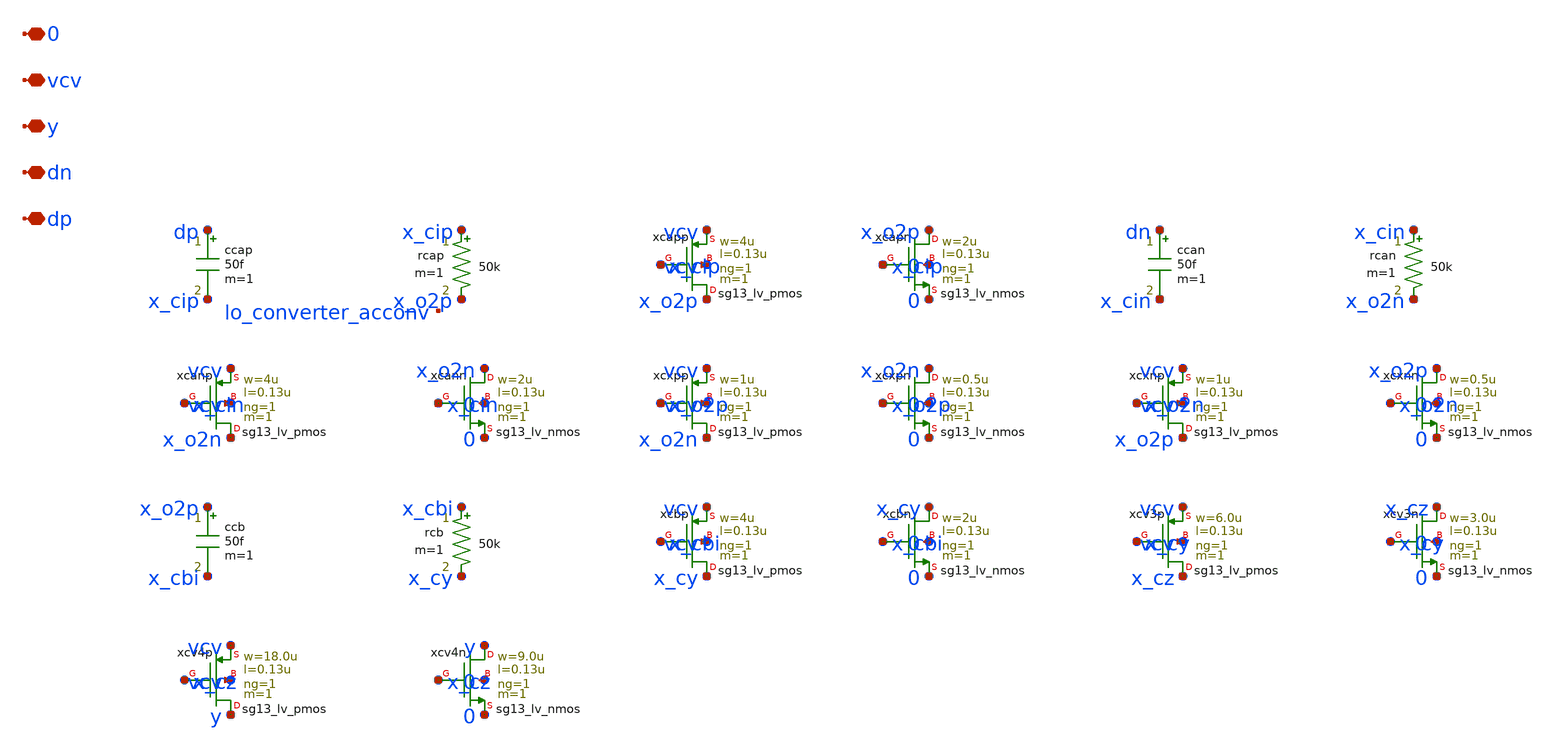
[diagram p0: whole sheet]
** sch_path: analog/lo/sch/lo_converter.sch
**.subckt lo_converter dp dn y vcv 0
*.iopin dp
*.iopin dn
*.iopin y
*.iopin vcv
*.iopin 0
ccap dp x_cip 50f m=1
rcap x_cip x_o2p 50k m=1
Xxcapp x_o2p x_cip vcv vcv sg13_lv_pmos w=4u l=0.13u ng=1 m=1 mm_ok=1
Xxcapn x_o2p x_cip 0 0 sg13_lv_nmos w=2u l=0.13u ng=1 m=1 mm_ok=1
ccan dn x_cin 50f m=1
rcan x_cin x_o2n 50k m=1
Xxcanp x_o2n x_cin vcv vcv sg13_lv_pmos w=4u l=0.13u ng=1 m=1 mm_ok=1
Xxcann x_o2n x_cin 0 0 sg13_lv_nmos w=2u l=0.13u ng=1 m=1 mm_ok=1
Xxcxpp x_o2n x_o2p vcv vcv sg13_lv_pmos w=1u l=0.13u ng=1 m=1 mm_ok=1
Xxcxpn x_o2n x_o2p 0 0 sg13_lv_nmos w=0.5u l=0.13u ng=1 m=1 mm_ok=1
Xxcxnp x_o2p x_o2n vcv vcv sg13_lv_pmos w=1u l=0.13u ng=1 m=1 mm_ok=1
Xxcxnn x_o2p x_o2n 0 0 sg13_lv_nmos w=0.5u l=0.13u ng=1 m=1 mm_ok=1
ccb x_o2p x_cbi 50f m=1
rcb x_cbi x_cy 50k m=1
Xxcbp x_cy x_cbi vcv vcv sg13_lv_pmos w=4u l=0.13u ng=1 m=1 mm_ok=1
Xxcbn x_cy x_cbi 0 0 sg13_lv_nmos w=2u l=0.13u ng=1 m=1 mm_ok=1
Xxcv3p x_cz x_cy vcv vcv sg13_lv_pmos w=6.0u l=0.13u ng=1 m=1 mm_ok=1
Xxcv3n x_cz x_cy 0 0 sg13_lv_nmos w=3.0u l=0.13u ng=1 m=1 mm_ok=1
Xxcv4p y x_cz vcv vcv sg13_lv_pmos w=18.0u l=0.13u ng=1 m=1 mm_ok=1
Xxcv4n y x_cz 0 0 sg13_lv_nmos w=9.0u l=0.13u ng=1 m=1 mm_ok=1
**.ends
.end
